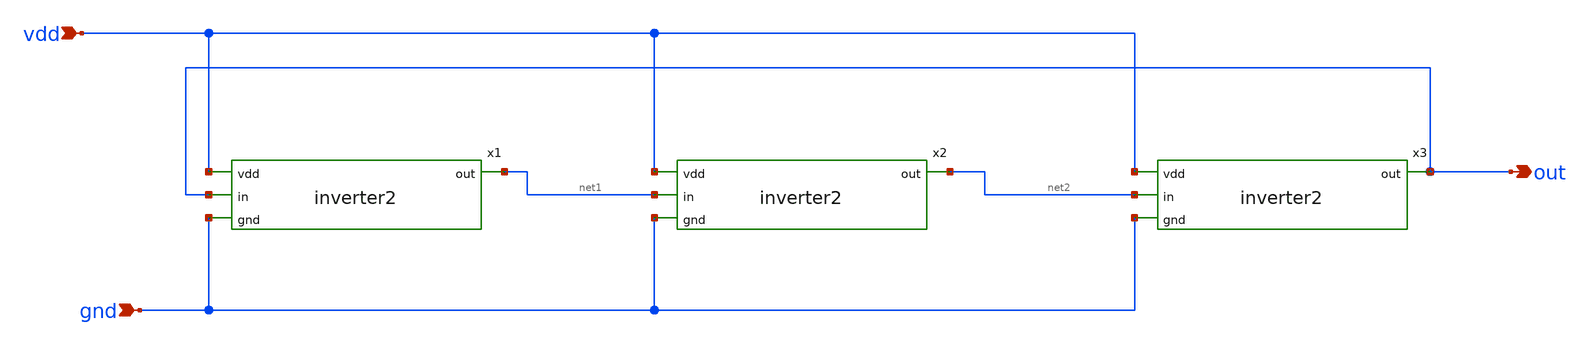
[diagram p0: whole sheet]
** sch_path: ringosc.sch
**.subckt ringosc out vdd gnd
*.opin out
*.ipin vdd
*.ipin gnd
x1 vdd out net1 gnd inverter2
x2 vdd net1 net2 gnd inverter2
x3 vdd net2 out gnd inverter2
**.ends

* expanding   symbol:  /home/nurlaela/MSIB/inverter2.sym # of pins=4
** sym_path: /home/nurlaela/MSIB/inverter2.sym
** sch_path: /home/nurlaela/MSIB/inverter2.sch
.subckt inverter2 vdd in out gnd
*.ipin in
*.opin out
*.ipin vdd
*.ipin gnd
XM1 out in gnd gnd sky130_fd_pr__nfet_01v8 L=0.15 W=0.5 nf=1 ad='int((nf+1)/2) * W/nf * 0.29' as='int((nf+2)/2) * W/nf * 0.29'
+ pd='2*int((nf+1)/2) * (W/nf + 0.29)' ps='2*int((nf+2)/2) * (W/nf + 0.29)' nrd='0.29 / W' nrs='0.29 / W'
+ sa=0 sb=0 sd=0 mult=1 m=1
XM2 out in vdd vdd sky130_fd_pr__pfet_01v8 L=0.15 W=0.5 nf=1 ad='int((nf+1)/2) * W/nf * 0.29' as='int((nf+2)/2) * W/nf * 0.29'
+ pd='2*int((nf+1)/2) * (W/nf + 0.29)' ps='2*int((nf+2)/2) * (W/nf + 0.29)' nrd='0.29 / W' nrs='0.29 / W'
+ sa=0 sb=0 sd=0 mult=1 m=1
.ends

.end
